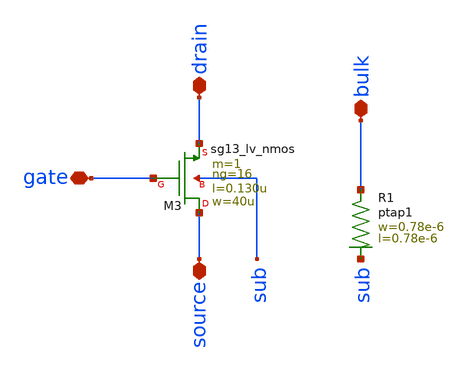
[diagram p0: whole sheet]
** sch_path: ts_pr_May2024/design_data/xschem/nmos16.sch
**.subckt nmos16 drain source bulk gate
*.iopin drain
*.iopin source
*.iopin bulk
*.iopin gate
XR1 bulk sub ptap1 R=262.8 w=0.78e-6 l=0.78e-6
XM3 source gate drain sub sg13_lv_nmos w=40u l=0.130u ng=16 m=1 mm_ok=1
**.ends
.end
